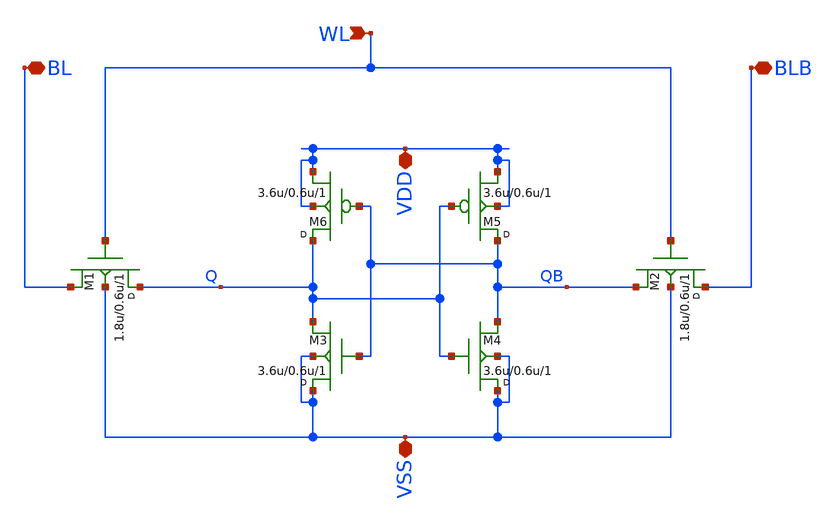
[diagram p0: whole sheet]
** sch_path: SRAM/cell/schematic/sram_cell_schematic.sch
**.subckt sram_cell_schematic WL BL BLB VDD VSS
*.ipin WL
*.iopin BL
*.iopin BLB
*.iopin VDD
*.iopin VSS
M4 VSS Q QB VSS nfet w=3.6u l=0.6u m=1
M5 QB Q VDD VDD pfet w=3.6u l=0.6u m=1
M6 Q QB VDD VDD pfet w=3.6u l=0.6u m=1
M1 Q WL BL VSS nfet w=1.8u l=0.6u m=1
M3 VSS QB Q VSS nfet w=3.6u l=0.6u m=1
M2 BLB WL QB VSS nfet w=1.8u l=0.6u m=1
**.ends
.end
